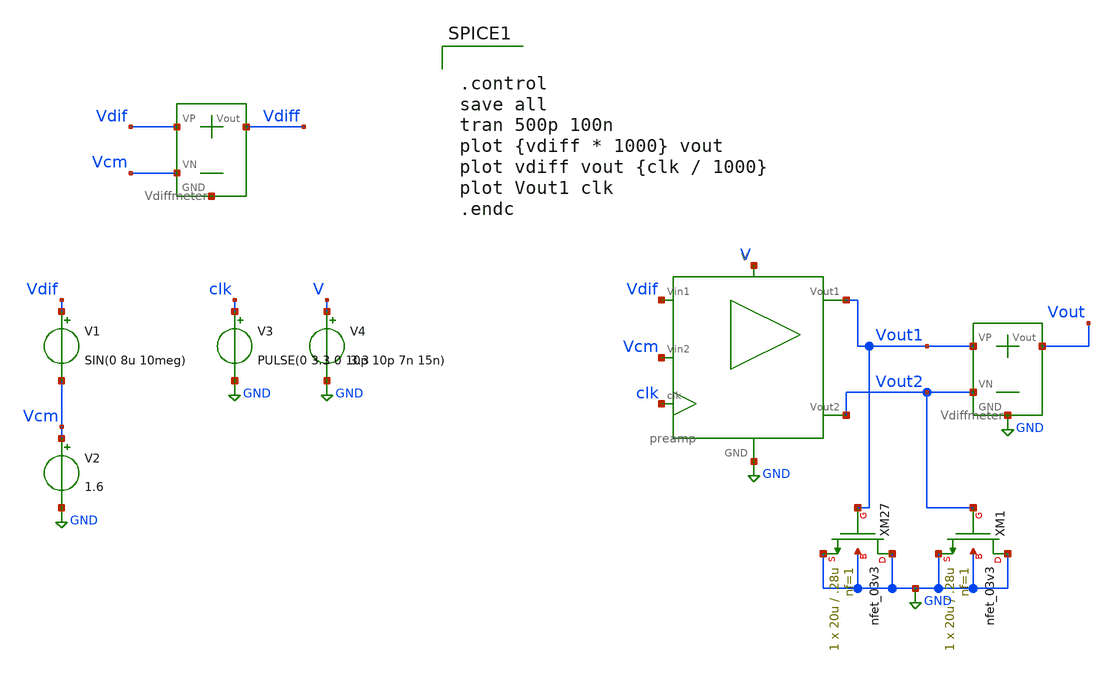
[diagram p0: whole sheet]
** sch_path: SAR_ADC/xschem/test/preamp_tb/sin_8u__tb.sch
**.subckt sin_8u__tb
V1 Vdif Vcm SIN(0 8u 10meg)
V2 Vcm GND 1.6
V3 clk GND PULSE(0 3.3 0 10p 10p 7n 15n)
V4 V GND 3.3
XM27 GND Vout1 GND GND nfet_03v3 L=.28u W=20u nf=1 ad='int((nf+1)/2) * W/nf * 0.18u' as='int((nf+2)/2) * W/nf * 0.18u'
+ pd='2*int((nf+1)/2) * (W/nf + 0.18u)' ps='2*int((nf+2)/2) * (W/nf + 0.18u)' nrd='0.18u / W' nrs='0.18u / W'
+ sa=0 sb=0 sd=0 m=1
XM1 GND Vout2 GND GND nfet_03v3 L=.28u W=20u nf=1 ad='int((nf+1)/2) * W/nf * 0.18u' as='int((nf+2)/2) * W/nf * 0.18u'
+ pd='2*int((nf+1)/2) * (W/nf + 0.18u)' ps='2*int((nf+2)/2) * (W/nf + 0.18u)' nrd='0.18u / W' nrs='0.18u / W'
+ sa=0 sb=0 sd=0 m=1
X1 V GND Vdif clk Vout1 Vout2 Vcm preamp
X2 Vdif Vcm Vdiff net1 Vdiffmeter
X3 Vout1 Vout2 Vout GND Vdiffmeter
**** begin user architecture code


.control
save all
tran 500p 100n
plot {vdiff * 1000} vout
plot vdiff vout {clk / 1000}
plot Vout1 clk
.endc


.include /foss/pdks/gf180mcuC/libs.tech/ngspice/design.ngspice
.lib /foss/pdks/gf180mcuC/libs.tech/ngspice/sm141064.ngspice typical

**** end user architecture code
**.ends

* expanding   symbol:  ../../../symbols/preamp.sym # of pins=7
** sym_path: SAR_ADC/xschem/designs/preamp.sym
** sch_path: SAR_ADC/xschem/designs/preamp.sch
.subckt preamp V GND Vin1 clk Vout1 Vout2 Vin2
*.iopin V
*.iopin GND
*.iopin Vout2
*.iopin Vout1
*.iopin clk
*.iopin Vin2
*.iopin Vin1
XM26 Vout2 clk GND GND nfet_03v3 L=.5u W=.22u nf=1 ad='int((nf+1)/2) * W/nf * 0.18u' as='int((nf+2)/2) * W/nf * 0.18u'
+ pd='2*int((nf+1)/2) * (W/nf + 0.18u)' ps='2*int((nf+2)/2) * (W/nf + 0.18u)' nrd='0.18u / W' nrs='0.18u / W'
+ sa=0 sb=0 sd=0 m=1
XM27 Vout1 clk GND GND nfet_03v3 L=.5u W=.22u nf=1 ad='int((nf+1)/2) * W/nf * 0.18u' as='int((nf+2)/2) * W/nf * 0.18u'
+ pd='2*int((nf+1)/2) * (W/nf + 0.18u)' ps='2*int((nf+2)/2) * (W/nf + 0.18u)' nrd='0.18u / W' nrs='0.18u / W'
+ sa=0 sb=0 sd=0 m=1
XM24 Vout1 Vin2 net1 V pfet_03v3 L=.28u W=8u nf=1 ad='int((nf+1)/2) * W/nf * 0.18u' as='int((nf+2)/2) * W/nf * 0.18u'
+ pd='2*int((nf+1)/2) * (W/nf + 0.18u)' ps='2*int((nf+2)/2) * (W/nf + 0.18u)' nrd='0.18u / W' nrs='0.18u / W'
+ sa=0 sb=0 sd=0 m=1
XM25 Vout2 Vin1 net1 V pfet_03v3 L=.28u W=8u nf=1 ad='int((nf+1)/2) * W/nf * 0.18u' as='int((nf+2)/2) * W/nf * 0.18u'
+ pd='2*int((nf+1)/2) * (W/nf + 0.18u)' ps='2*int((nf+2)/2) * (W/nf + 0.18u)' nrd='0.18u / W' nrs='0.18u / W'
+ sa=0 sb=0 sd=0 m=1
XM1 V clk net1 V pfet_03v3 L=2u W=1u nf=1 ad='int((nf+1)/2) * W/nf * 0.18u' as='int((nf+2)/2) * W/nf * 0.18u'
+ pd='2*int((nf+1)/2) * (W/nf + 0.18u)' ps='2*int((nf+2)/2) * (W/nf + 0.18u)' nrd='0.18u / W' nrs='0.18u / W'
+ sa=0 sb=0 sd=0 m=1
.ends


* expanding   symbol:  ../../../symbols/Vdiffmeter.sym # of pins=4
** sym_path: SAR_ADC/xschem/spice/symbols/Vdiffmeter.sym
** sch_path: SAR_ADC/xschem/spice/symbols/Vdiffmeter.sch
.subckt Vdiffmeter VP VN Vout GND
*.iopin Vout
*.iopin GND
*.iopin VP
*.iopin VN
R4 Vout GND 1k m=1
E4 Vout GND VP VN 1
.ends

.GLOBAL GND
.end
